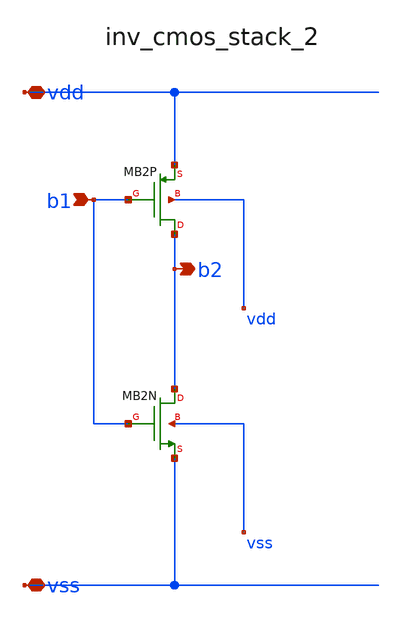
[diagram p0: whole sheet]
** sch_path: analog-db/raw/cmp_001_hyst_diffpair/hier/blocks/inv_cmos_stack_2.sch
**.subckt inv_cmos_stack_2 b1 vdd vss b2
*.ipin b1
*.iopin vdd
*.iopin vss
*.opin b2
XMB2N b2 b1 vss vss sg13_lv_nmos w=x_dut_xmb2n_w l=x_dut_xmb2n_l ng=1 m=x_dut_xmb2n_m
XMB2P b2 b1 vdd vdd sg13_lv_pmos w=x_dut_xmb2p_w l=x_dut_xmb2p_l ng=1 m=x_dut_xmb2p_m
**.ends
.end
